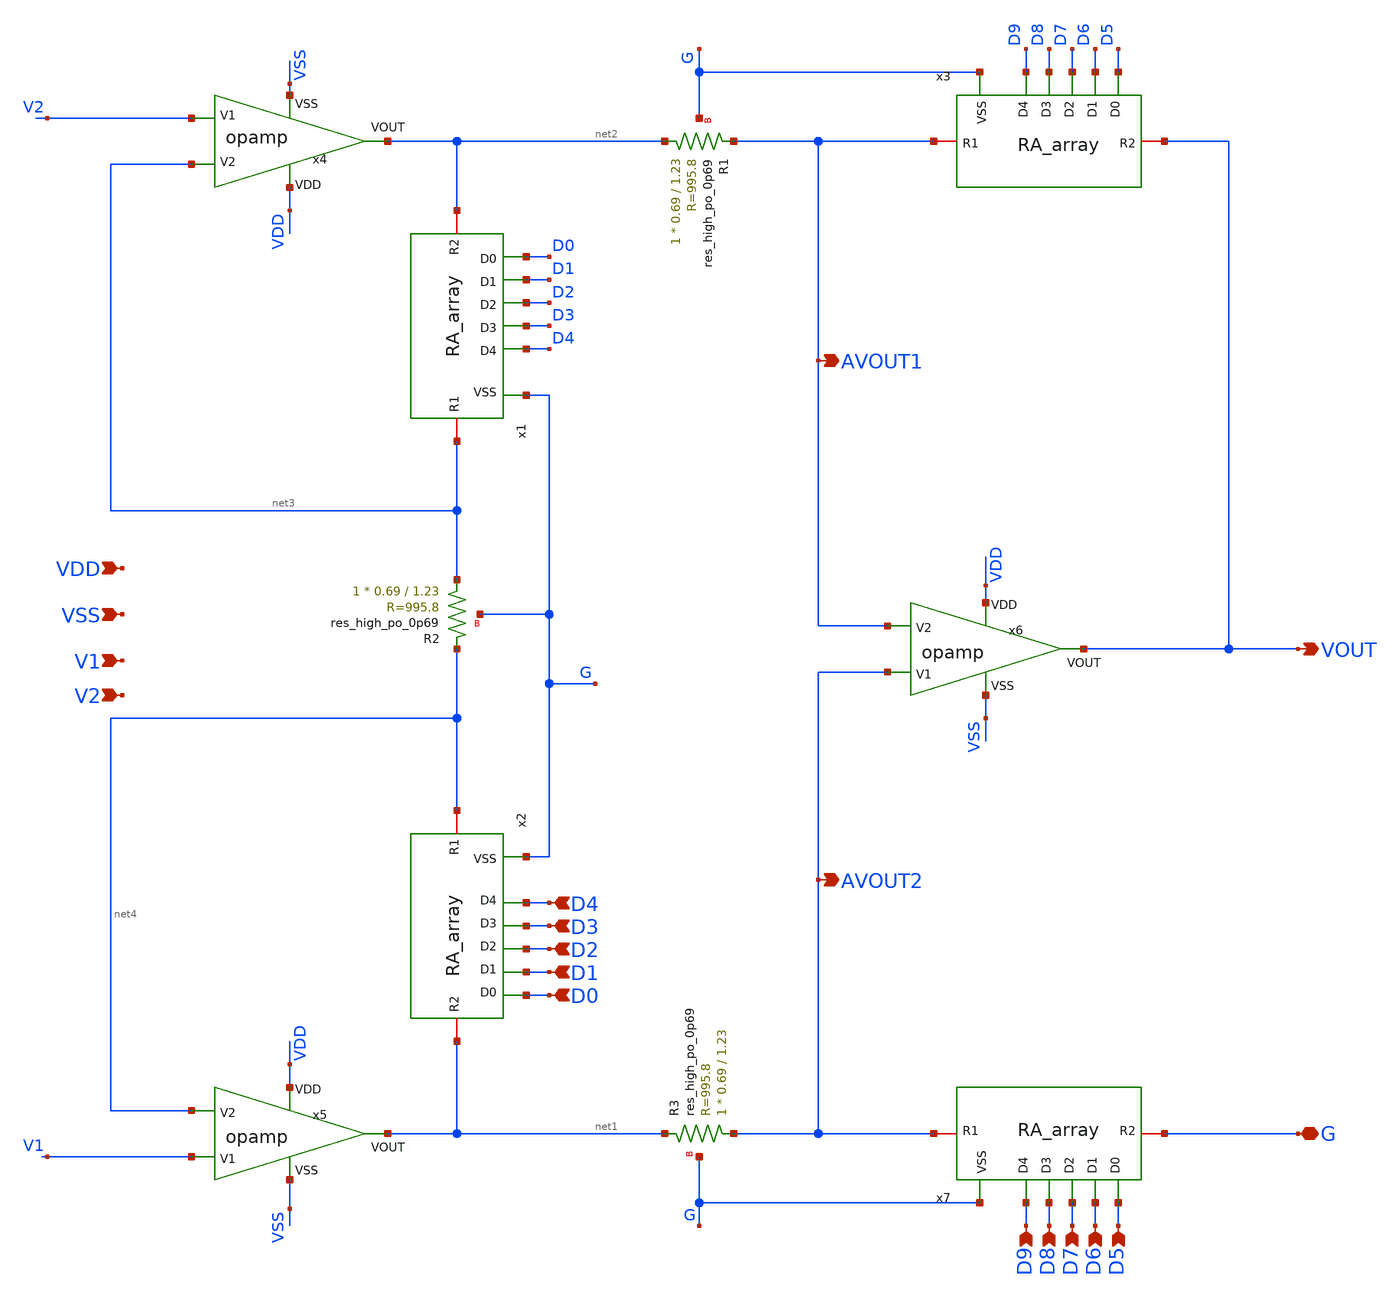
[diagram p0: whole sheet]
** sch_path: xschem/IA_v2.sch
**.subckt IA_v2 VOUT G VDD VSS V1 V2 D4 D3 D2 D1 D0 D9 D8 D7 D6 D5 AVOUT1 AVOUT2
*.opin VOUT
*.iopin G
*.ipin VDD
*.ipin VSS
*.ipin V1
*.ipin V2
*.ipin D4
*.ipin D3
*.ipin D2
*.ipin D1
*.ipin D0
*.ipin D9
*.ipin D8
*.ipin D7
*.ipin D6
*.ipin D5
*.opin AVOUT1
*.opin AVOUT2
x4 VDD VSS V2 net3 net2 opamp
x5 VDD VSS V1 net4 net1 opamp
x6 VDD VSS AVOUT2 AVOUT1 VOUT opamp
x1 G net3 net2 D0 D1 D2 D3 D4 RA_array
x2 G net4 net1 D0 D1 D2 D3 D4 RA_array
x3 G AVOUT1 VOUT D5 D6 D7 D8 D9 RA_array
x7 G AVOUT2 G D5 D6 D7 D8 D9 RA_array
XR1 net2 AVOUT1 G sky130_fd_pr__res_high_po_0p69 L=1.23 mult=1 m=1
XR2 net3 net4 G sky130_fd_pr__res_high_po_0p69 L=1.23 mult=1 m=1
XR3 AVOUT2 net1 G sky130_fd_pr__res_high_po_0p69 L=1.23 mult=1 m=1
**.ends
.end
